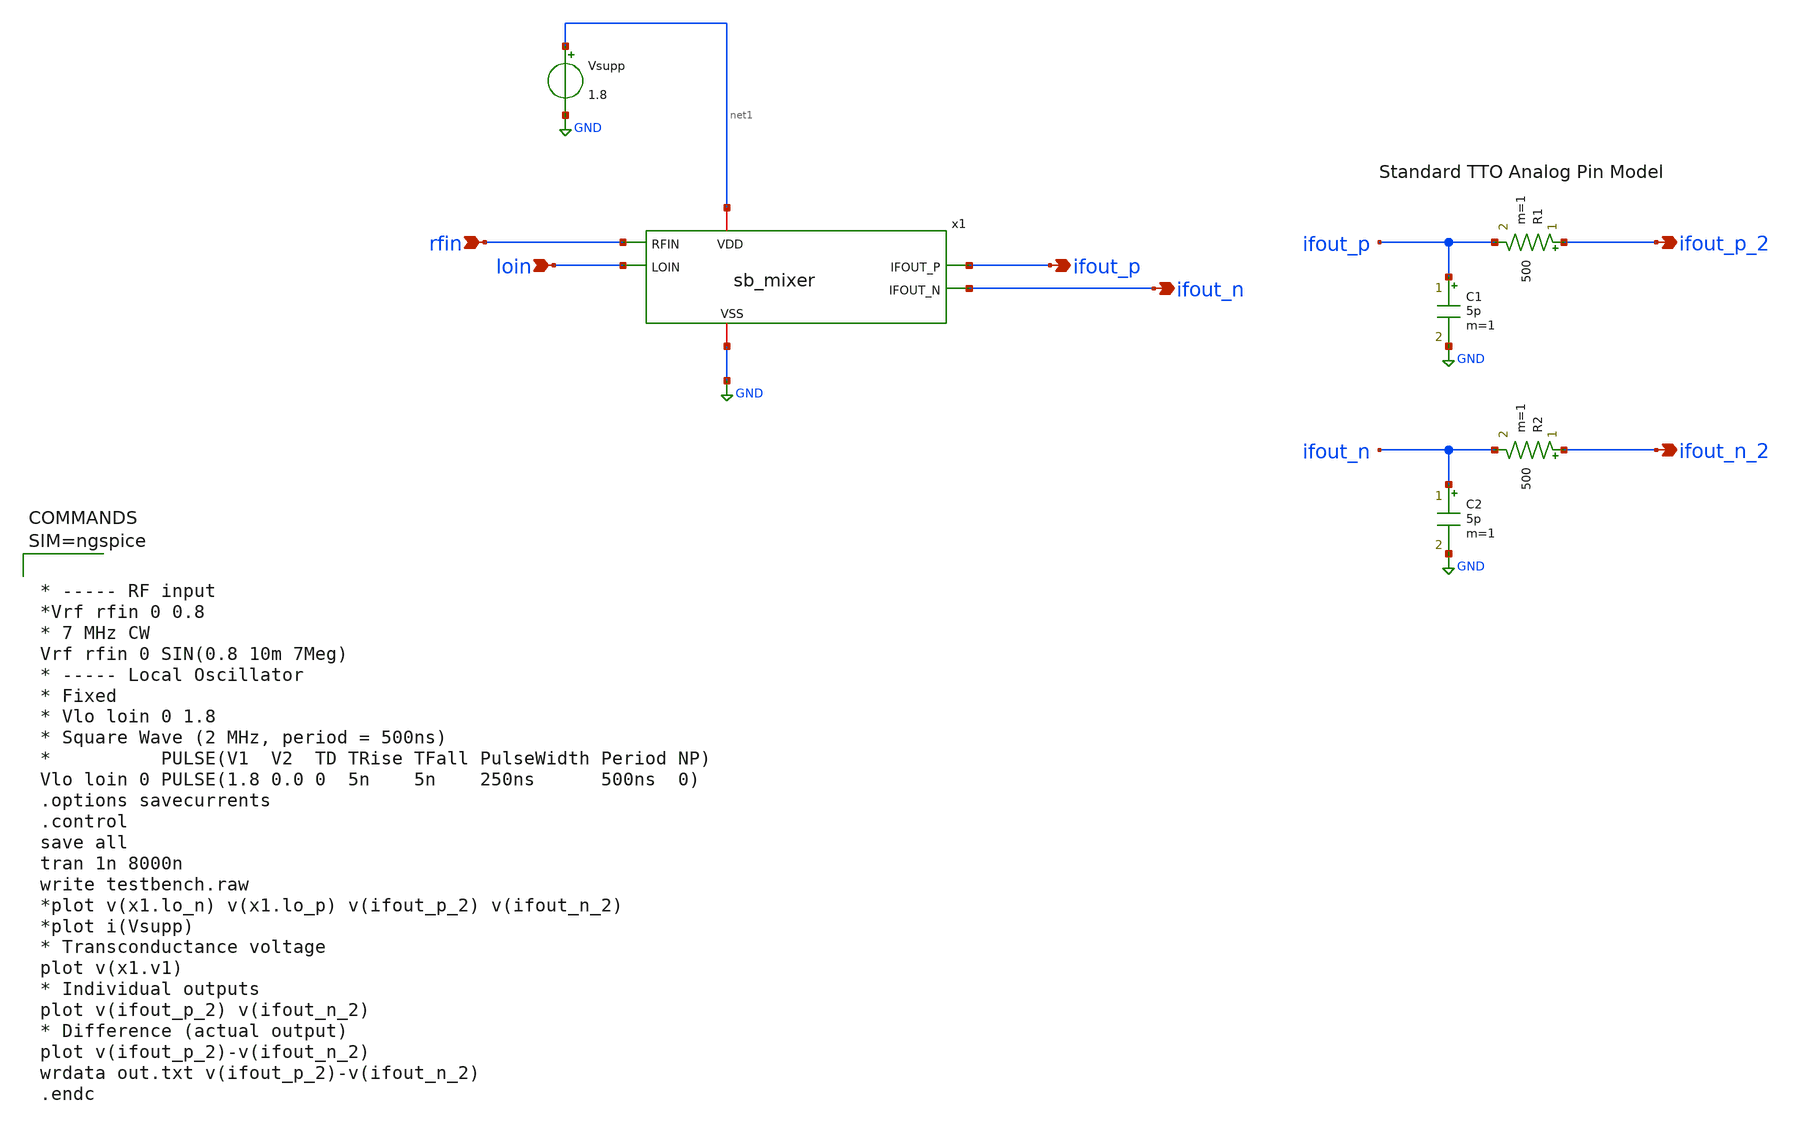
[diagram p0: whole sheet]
** sch_path: xschem/testbench.sch
**.subckt testbench loin rfin ifout_p ifout_n ifout_p_2 ifout_n_2
*.ipin loin
*.ipin rfin
*.opin ifout_p
*.opin ifout_n
*.opin ifout_p_2
*.opin ifout_n_2
x1 ifout_p ifout_n rfin net1 GND loin sb_mixer
C1 ifout_p GND 5p m=1
R1 ifout_p_2 ifout_p 500 m=1
C2 ifout_n GND 5p m=1
R2 ifout_n_2 ifout_n 500 m=1
Vsupp net1 GND 1.8
**** begin user architecture code

** opencircuitdesign pdks install
.lib $::SKYWATER_MODELS/sky130.lib.spice tt
.include $::SKYWATER_STDCELLS/sky130_fd_sc_hd.spice





* ----- RF input
*Vrf rfin 0 0.8
* 7 MHz CW
Vrf rfin 0 SIN(0.8 10m 7Meg)
* ----- Local Oscillator
* Fixed
* Vlo loin 0 1.8
* Square Wave (2 MHz, period = 500ns)
*          PULSE(V1  V2  TD TRise TFall PulseWidth Period NP)
Vlo loin 0 PULSE(1.8 0.0 0  5n    5n    250ns      500ns  0)
.options savecurrents
.control
save all
tran 1n 8000n
write testbench.raw
*plot v(x1.lo_n) v(x1.lo_p) v(ifout_p_2) v(ifout_n_2)
*plot i(Vsupp)
* Transconductance voltage
plot v(x1.v1)
* Individual outputs
plot v(ifout_p_2) v(ifout_n_2)
* Difference (actual output)
plot v(ifout_p_2)-v(ifout_n_2)
wrdata out.txt v(ifout_p_2)-v(ifout_n_2)
.endc



**** end user architecture code
**.ends

* expanding   symbol:  sb_mixer.sym # of pins=6
** sym_path: xschem/sb_mixer.sym
** sch_path: xschem/sb_mixer.sch
.subckt sb_mixer IFOUT_P IFOUT_N RFIN VDD VSS LOIN
*.iopin VDD
*.iopin VSS
*.ipin LOIN
*.ipin RFIN
*.opin IFOUT_P
*.opin IFOUT_N
x1 LOIN VSS VSS VDD VDD LO_N sky130_fd_sc_hd__inv_1
x2 LO_N VSS VSS VDD VDD LO_P sky130_fd_sc_hd__inv_1
XM1 V1 RFIN VSS VSS sky130_fd_pr__nfet_01v8_lvt L=2 W=20 nf=4 ad='int((nf+1)/2) * W/nf * 0.29' as='int((nf+2)/2) * W/nf * 0.29'
+ pd='2*int((nf+1)/2) * (W/nf + 0.29)' ps='2*int((nf+2)/2) * (W/nf + 0.29)' nrd='0.29 / W' nrs='0.29 / W'
+ sa=0 sb=0 sd=0 mult=1 m=1
XM2 IFOUT_P LO_P V1 VSS sky130_fd_pr__nfet_01v8 L=2 W=10 nf=2 ad='int((nf+1)/2) * W/nf * 0.29' as='int((nf+2)/2) * W/nf * 0.29'
+ pd='2*int((nf+1)/2) * (W/nf + 0.29)' ps='2*int((nf+2)/2) * (W/nf + 0.29)' nrd='0.29 / W' nrs='0.29 / W'
+ sa=0 sb=0 sd=0 mult=1 m=1
XM3 IFOUT_N LO_N V1 VSS sky130_fd_pr__nfet_01v8 L=2 W=10 nf=2 ad='int((nf+1)/2) * W/nf * 0.29' as='int((nf+2)/2) * W/nf * 0.29'
+ pd='2*int((nf+1)/2) * (W/nf + 0.29)' ps='2*int((nf+2)/2) * (W/nf + 0.29)' nrd='0.29 / W' nrs='0.29 / W'
+ sa=0 sb=0 sd=0 mult=1 m=1
XR1 IFOUT_P VDD VSS sky130_fd_pr__res_high_po_0p69 L=0.69 mult=1 m=1
XR2 IFOUT_N VDD VSS sky130_fd_pr__res_high_po_0p69 L=0.69 mult=1 m=1
.ends

.GLOBAL GND
.end
